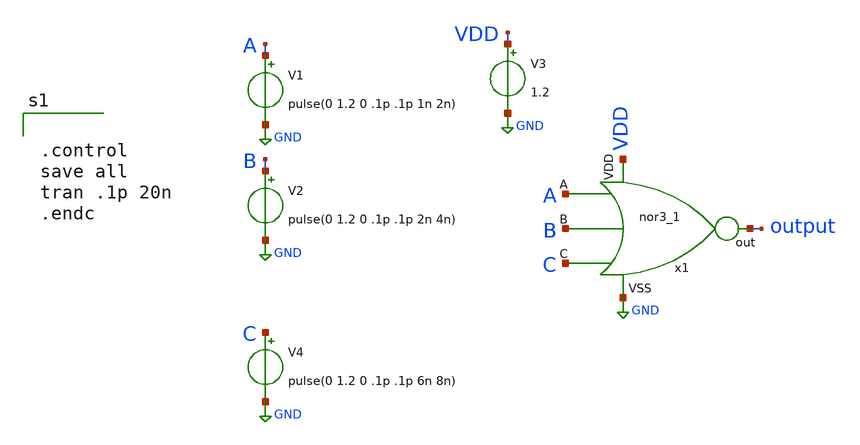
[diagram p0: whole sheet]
** sch_path: nor/nor3_tb.sch
**.subckt nor3_tb
V1 A GND pulse(0 1.2 0 .1p .1p 1n 2n)
V2 B GND pulse(0 1.2 0 .1p .1p 2n 4n)
V3 VDD GND 1.2
x1 VDD A B C output GND nor3
V4 C GND pulse(0 1.2 0 .1p .1p 6n 8n)
**** begin user architecture code

** opencircuitdesign pdks install
.lib $::SKYWATER_MODELS/sky130.lib.spice tt




.control
save all
tran .1p 20n
.endc

**** end user architecture code
**.ends

* expanding   symbol:  nor3.sym # of pins=6
** sym_path: nor/nor3.sym
** sch_path: nor/nor3.sch
.subckt nor3 VDD A B C out VSS
*.ipin A
*.ipin B
*.opin out
*.ipin VSS
*.ipin VDD
*.ipin C
XM1 out B VSS VSS sky130_fd_pr__nfet_01v8 L=0.15 W=1 nf=1 ad='int((nf+1)/2) * W/nf * 0.29' as='int((nf+2)/2) * W/nf * 0.29'
+ pd='2*int((nf+1)/2) * (W/nf + 0.29)' ps='2*int((nf+2)/2) * (W/nf + 0.29)' nrd='0.29 / W' nrs='0.29 / W'
+ sa=0 sb=0 sd=0 mult=1 m=1
XM2 net2 B net1 net1 sky130_fd_pr__pfet_01v8 L=0.15 W=1 nf=1 ad='int((nf+1)/2) * W/nf * 0.29' as='int((nf+2)/2) * W/nf * 0.29'
+ pd='2*int((nf+1)/2) * (W/nf + 0.29)' ps='2*int((nf+2)/2) * (W/nf + 0.29)' nrd='0.29 / W' nrs='0.29 / W'
+ sa=0 sb=0 sd=0 mult=1 m=1
XM3 net1 A VDD VDD sky130_fd_pr__pfet_01v8 L=0.15 W=1 nf=1 ad='int((nf+1)/2) * W/nf * 0.29' as='int((nf+2)/2) * W/nf * 0.29'
+ pd='2*int((nf+1)/2) * (W/nf + 0.29)' ps='2*int((nf+2)/2) * (W/nf + 0.29)' nrd='0.29 / W' nrs='0.29 / W'
+ sa=0 sb=0 sd=0 mult=1 m=1
XM4 out A VSS VSS sky130_fd_pr__nfet_01v8 L=0.15 W=1 nf=1 ad='int((nf+1)/2) * W/nf * 0.29' as='int((nf+2)/2) * W/nf * 0.29'
+ pd='2*int((nf+1)/2) * (W/nf + 0.29)' ps='2*int((nf+2)/2) * (W/nf + 0.29)' nrd='0.29 / W' nrs='0.29 / W'
+ sa=0 sb=0 sd=0 mult=1 m=1
XM5 out C net2 net2 sky130_fd_pr__pfet_01v8 L=0.15 W=1 nf=1 ad='int((nf+1)/2) * W/nf * 0.29' as='int((nf+2)/2) * W/nf * 0.29'
+ pd='2*int((nf+1)/2) * (W/nf + 0.29)' ps='2*int((nf+2)/2) * (W/nf + 0.29)' nrd='0.29 / W' nrs='0.29 / W'
+ sa=0 sb=0 sd=0 mult=1 m=1
XM6 out C VSS VSS sky130_fd_pr__nfet_01v8 L=0.15 W=1 nf=1 ad='int((nf+1)/2) * W/nf * 0.29' as='int((nf+2)/2) * W/nf * 0.29'
+ pd='2*int((nf+1)/2) * (W/nf + 0.29)' ps='2*int((nf+2)/2) * (W/nf + 0.29)' nrd='0.29 / W' nrs='0.29 / W'
+ sa=0 sb=0 sd=0 mult=1 m=1
.ends

.GLOBAL GND
.end
